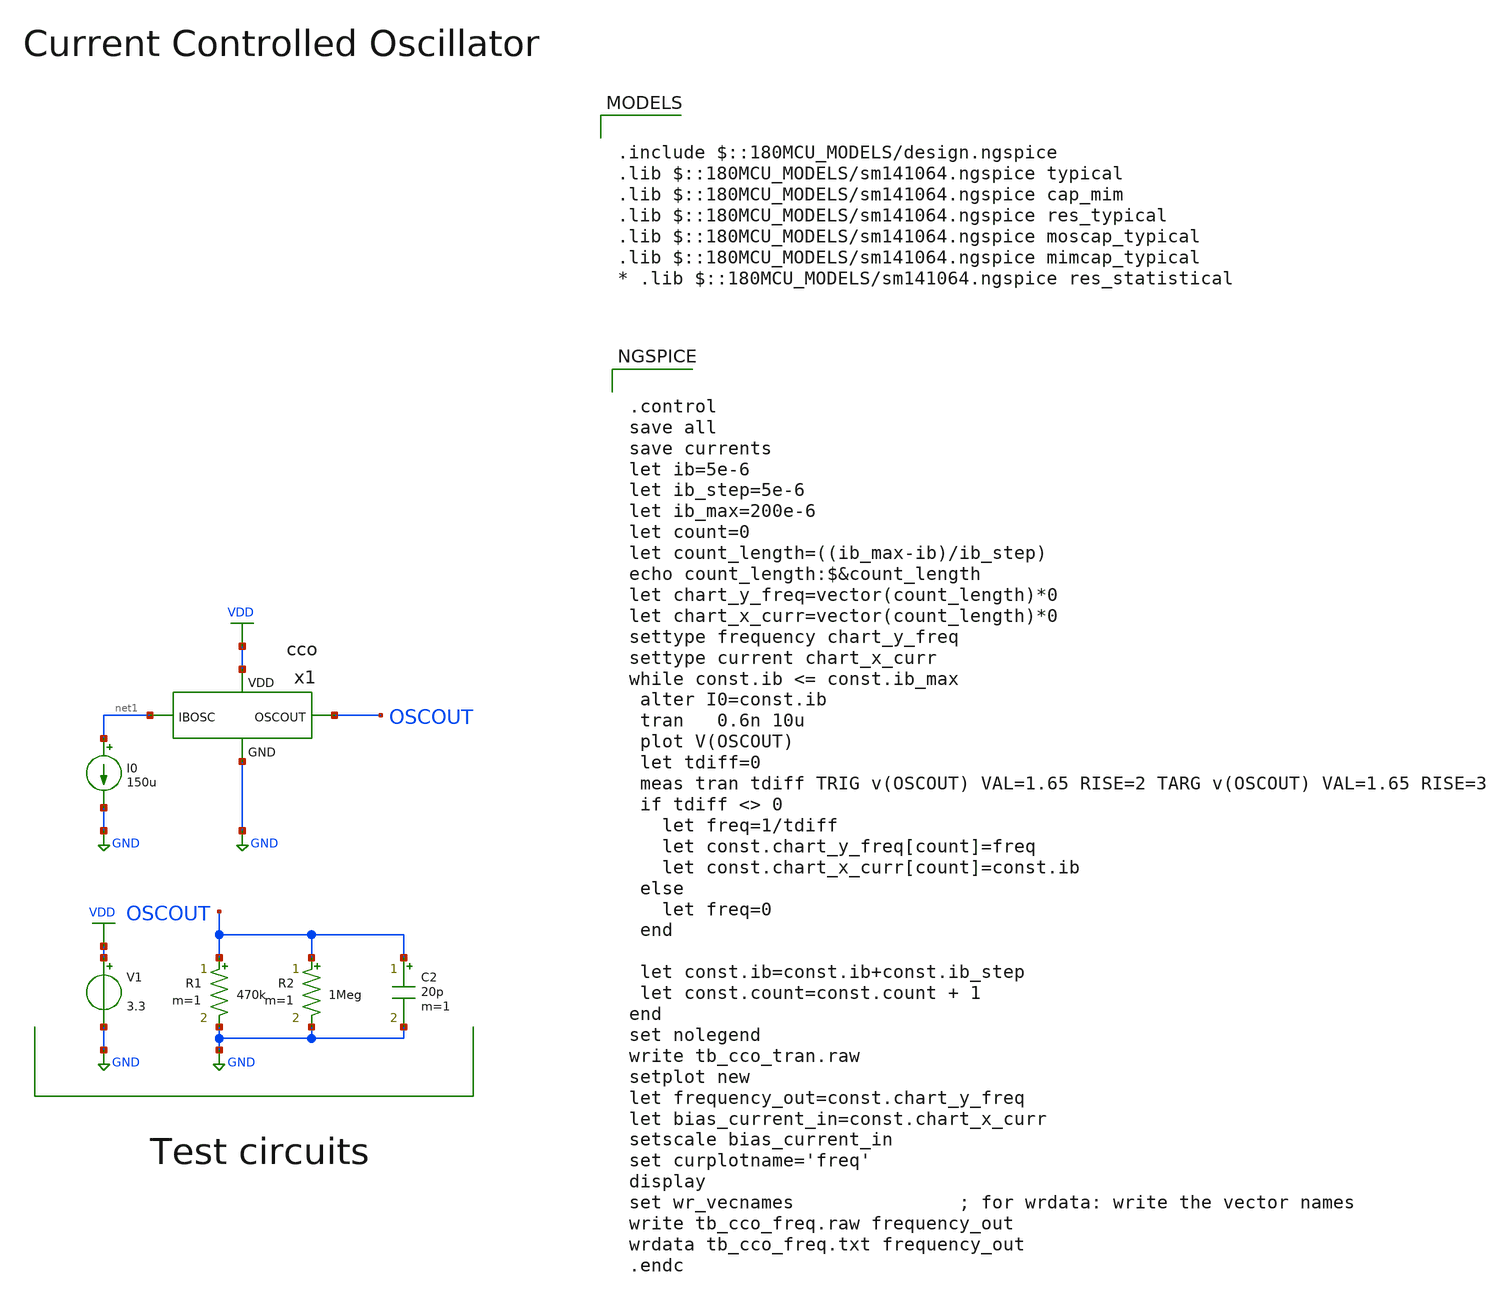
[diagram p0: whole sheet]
** sch_path: designs/libs/tb_analog/tb_cco/tb_cco_tran.sch
* Copyright 2022 GlobalFoundries PDK Authors
* Licensed under the Apache License, Version 2.0 (the "License");
* you may not use this file except in compliance with the License.
* You may obtain a copy of the License at
* https://www.apache.org/licenses/LICENSE-2.0
* Unless required by applicable law or agreed to in writing, software
* distributed under the License is distributed on an "AS IS" BASIS,
* WITHOUT WARRANTIES OR CONDITIONS OF ANY KIND, either express or implied.
* See the License for the specific language governing permissions and
* limitations under the License.
**.subckt tb_cco_tran
V1 VDD GND 3.3
I0 net1 GND 150u
R1 OSCOUT GND 470k m=1
R2 OSCOUT GND 1Meg m=1
C2 OSCOUT GND 20p m=1
x1 VDD GND net1 OSCOUT cco
**** begin user architecture code


.control
save all
save currents
let ib=5e-6
let ib_step=5e-6
let ib_max=200e-6
let count=0
let count_length=((ib_max-ib)/ib_step)
echo count_length:$&count_length
let chart_y_freq=vector(count_length)*0
let chart_x_curr=vector(count_length)*0
settype frequency chart_y_freq
settype current chart_x_curr
while const.ib <= const.ib_max
 alter I0=const.ib
 tran   0.6n 10u
 plot V(OSCOUT)
 let tdiff=0
 meas tran tdiff TRIG v(OSCOUT) VAL=1.65 RISE=2 TARG v(OSCOUT) VAL=1.65 RISE=3
 if tdiff <> 0
   let freq=1/tdiff
   let const.chart_y_freq[count]=freq
   let const.chart_x_curr[count]=const.ib
 else
   let freq=0
 end

 let const.ib=const.ib+const.ib_step
 let const.count=const.count + 1
end
set nolegend
write tb_cco_tran.raw
setplot new
let frequency_out=const.chart_y_freq
let bias_current_in=const.chart_x_curr
setscale bias_current_in
set curplotname='freq'
display
set wr_vecnames               ; for wrdata: write the vector names
write tb_cco_freq.raw frequency_out
wrdata tb_cco_freq.txt frequency_out
.endc



.include $::180MCU_MODELS/design.ngspice
.lib $::180MCU_MODELS/sm141064.ngspice typical
.lib $::180MCU_MODELS/sm141064.ngspice cap_mim
.lib $::180MCU_MODELS/sm141064.ngspice res_typical
.lib $::180MCU_MODELS/sm141064.ngspice moscap_typical
.lib $::180MCU_MODELS/sm141064.ngspice mimcap_typical
* .lib $::180MCU_MODELS/sm141064.ngspice res_statistical

**** end user architecture code
**.ends
.GLOBAL VDD
.GLOBAL GND
.end
